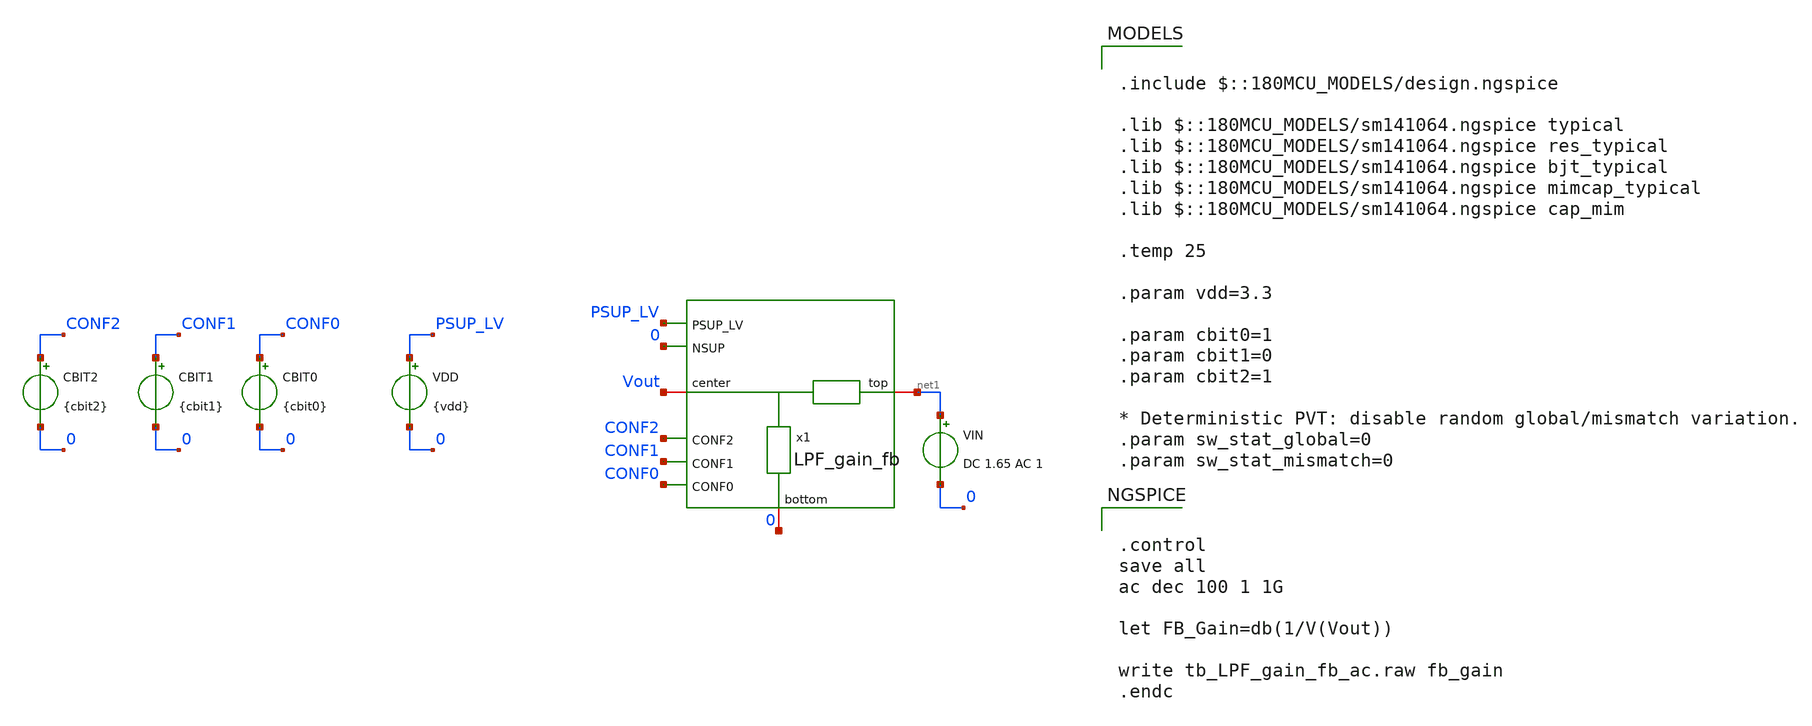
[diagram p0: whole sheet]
** sch_path: xschem/blocks/LPF_gain_fb/tb_LPF_gain_fb_ac.sch
**.subckt tb_LPF_gain_fb_ac
VDD PSUP_LV 0 {vdd}
x1 net1 Vout PSUP_LV 0 CONF2 CONF1 CONF0 0 LPF_gain_fb
VIN net1 0 DC 1.65 AC 1
CBIT2 CONF2 0 {cbit2}
CBIT1 CONF1 0 {cbit1}
CBIT0 CONF0 0 {cbit0}
**** begin user architecture code

.include $::180MCU_MODELS/design.ngspice

.lib $::180MCU_MODELS/sm141064.ngspice typical
.lib $::180MCU_MODELS/sm141064.ngspice res_typical
.lib $::180MCU_MODELS/sm141064.ngspice bjt_typical
.lib $::180MCU_MODELS/sm141064.ngspice mimcap_typical
.lib $::180MCU_MODELS/sm141064.ngspice cap_mim

.temp 25

.param vdd=3.3

.param cbit0=1
.param cbit1=0
.param cbit2=1

* Deterministic PVT: disable random global/mismatch variation.
.param sw_stat_global=0
.param sw_stat_mismatch=0



.control
save all
ac dec 100 1 1G

let FB_Gain=db(1/V(Vout))

write tb_LPF_gain_fb_ac.raw fb_gain
.endc


**** end user architecture code
**.ends
.end
